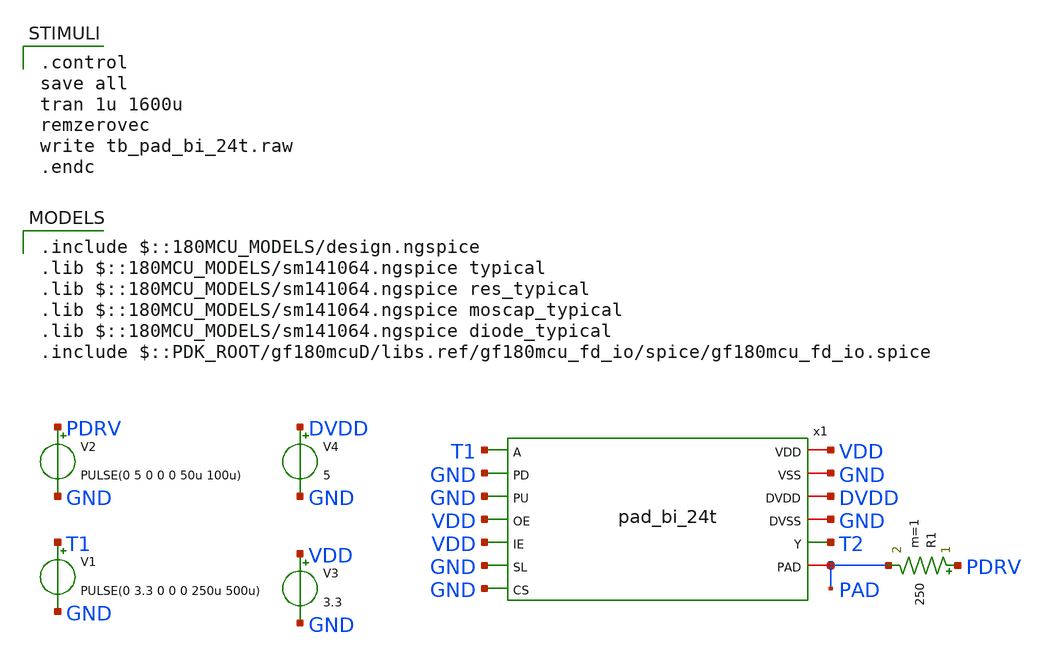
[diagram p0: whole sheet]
** sch_path: pads/tb_pad_bi_24t.sch
**.subckt tb_pad_bi_24t
x1 T1 GND GND VDD GND VDD VDD DVDD GND GND T2 PAD GND pad_bi_24t
V3 VDD GND 3.3
V1 T1 GND PULSE(0 3.3 0 0 0 250u 500u)
R1 PDRV PAD 250 m=1
V2 PDRV GND PULSE(0 5 0 0 0 50u 100u)
V4 DVDD GND 5
**** begin user architecture code
 .include $::180MCU_MODELS/design.ngspice
.lib $::180MCU_MODELS/sm141064.ngspice typical
.lib $::180MCU_MODELS/sm141064.ngspice res_typical
.lib $::180MCU_MODELS/sm141064.ngspice moscap_typical
.lib $::180MCU_MODELS/sm141064.ngspice diode_typical
.include $::PDK_ROOT/gf180mcuD/libs.ref/gf180mcu_fd_io/spice/gf180mcu_fd_io.spice


.control
save all
tran 1u 1600u
remzerovec
write tb_pad_bi_24t.raw
.endc

**** end user architecture code
**.ends

* expanding   symbol:  pad_bi_24t.sym # of pins=13
** sym_path: pads/pad_bi_24t.sym
.subckt pad_bi_24t A CS DVDD DVSS IE OE PAD PD PU SL VDD VSS Y
x1 A CS DVDD DVSS IE OE PAD PD PU SL VDD VSS Y gf180mcu_fd_io__bi_24t
.ends
.end
